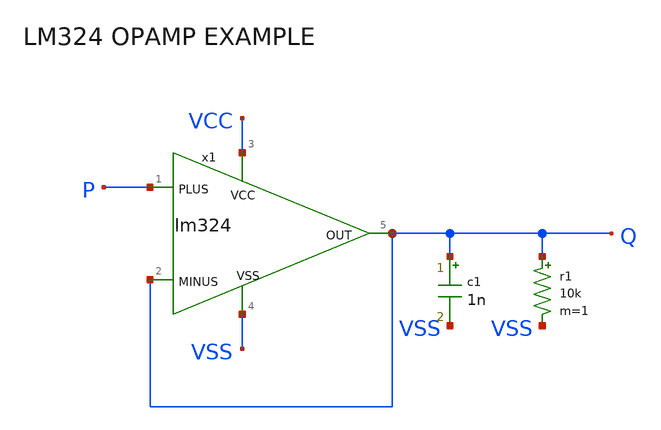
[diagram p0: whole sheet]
** sch_path: xschem_library/examples/test_lm324.sch
**.subckt test_lm324
x1 P Q VCC VSS Q lm324
r1 Q VSS 10k m=1
c1 Q VSS 1n m=1
**** begin user architecture code



.option RUNLVL=5 post
.param VCC=10
.param VSS=0
.temp  25
vvcc vcc 0 dc VCC
vvss vss 0 dc VSS
vp p 0 pwl 0 0 100n 2 200u 2 201u 3 400u 3 401u 1

.tran 0.1u 500u


**** end user architecture code
**.ends

* expanding   symbol:  examples/lm324.sym # of pins=5
** sym_path: xschem_library/examples/lm324.sym
** sch_path: xschem_library/examples/lm324.sch
.subckt lm324 1 2 3 4 5
*.ipin 1
*.ipin 2
*.ipin 3
*.ipin 4
*.opin 5
**** begin user architecture code
* LM324 OPERATIONAL AMPLIFIER "MACROMODEL" SUBCIRCUIT
* CREATED USING PARTS RELEASE 4.01 ON 09/08/89 AT 10:54
* (REV N/A)      SUPPLY VOLTAGE: 5V
* CONNECTIONS:   NON-INVERTING INPUT
*                | INVERTING INPUT
*                | | POSITIVE POWER SUPPLY
*                | | | NEGATIVE POWER SUPPLY
*                | | | | OUTPUT
*                | | | | |
* .SUBCKT LM324  1 2 3 4 5
*
  C1   11 12 5.544E-12
  C2    6  7 20.00E-12
  DC    5 53 DX
  DE   54  5 DX
  DLP  90 91 DX
  DLN  92 90 DX
  DP    4  3 DX
  EGND 99  0 POLY(2) (3,0) (4,0) 0 .5 .5
  FB    7 99 POLY(5) VB VC VE VLP VLN 0 15.91E6 -20E6 20E6 20E6 -20E6
  GA    6  0 11 12 125.7E-6
  GCM   0  6 10 99 7.067E-9
  IEE   3 10 DC 10.04E-6
  HLIM 90  0 VLIM 1K
  Q1   11  2 13 QX
  Q2   12  1 14 QX
  R2    6  9 100.0E3
  RC1   4 11 7.957E3
  RC2   4 12 7.957E3
  RE1  13 10 2.773E3
  RE2  14 10 2.773E3
  REE  10 99 19.92E6
  RO1   8  5 50
  RO2   7 99 50
  RP    3  4 30.31E3
  VB    9  0 DC 0
  VC 3 53 DC 2.100
  VE   54  4 DC .6
  VLIM  7  8 DC 0
  VLP  91  0 DC 40
  VLN   0 92 DC 40
.MODEL DX D(IS=800.0E-18)
.MODEL QX PNP(IS=800.0E-18 BF=250)
* .ENDS
**** end user architecture code
.ends

.end
